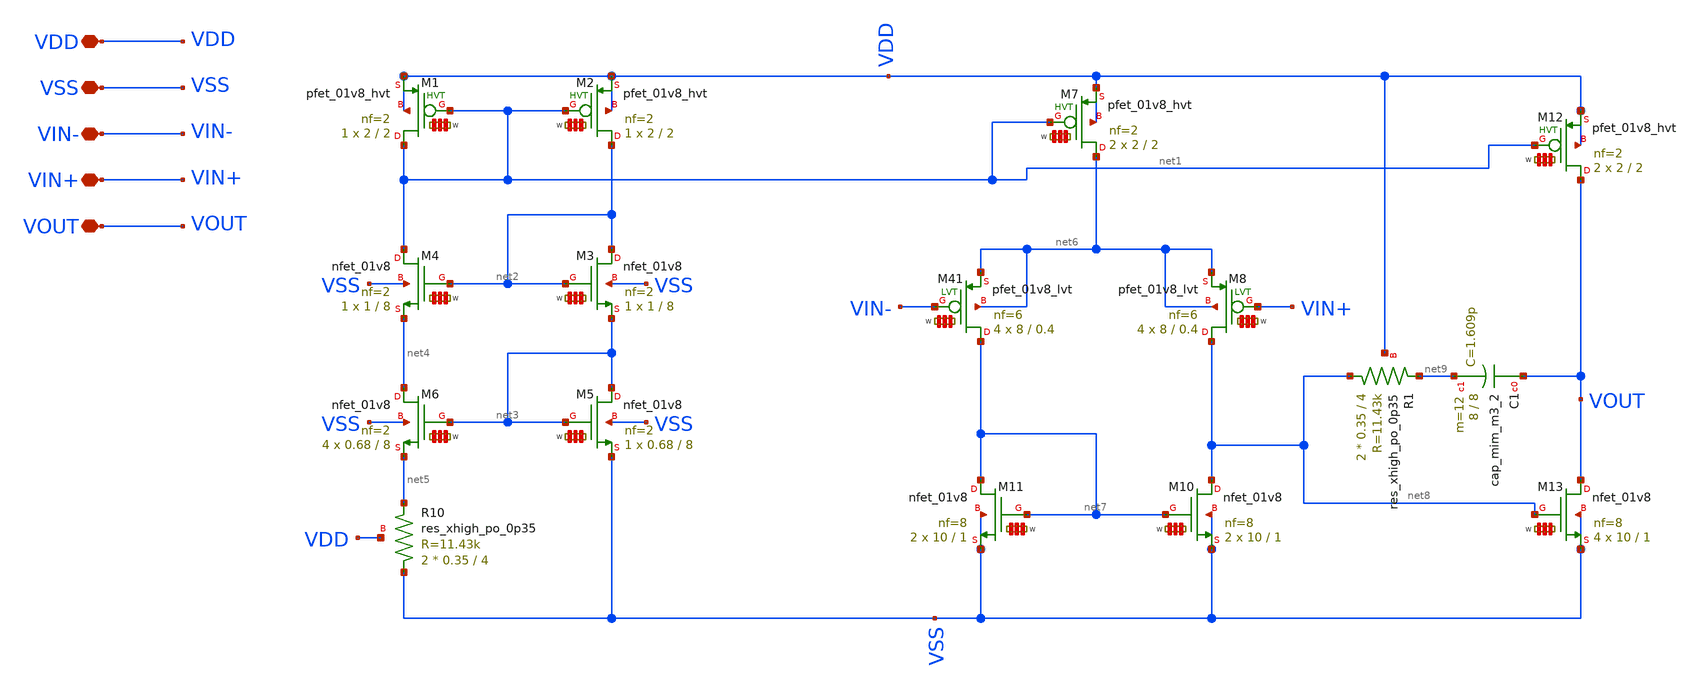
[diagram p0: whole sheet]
** sch_path: my_ip/sky130A/PMOS_2_stage_1_8_opamp_V1/op_amp.sch
**.subckt op_amp VDD VSS VIN- VIN+ VOUT
*.iopin VDD
*.iopin VSS
*.iopin VIN-
*.iopin VIN+
*.iopin VOUT
XM5 net3 net3 VSS VSS sky130_fd_pr__nfet_01v8 L=8 W='0.68 * 2 ' nf=2 ad='int((2 + 1)/2) * 0.68 / 2 * 0.29'
+ as='int((2 + 2)/2) * 0.68 / 2 * 0.29' pd='2*int((2 + 1)/2) * (0.68 / 2 + 0.29)' ps='2*int((2 + 2)/2) * (0.68 / 2 + 0.29)'
+ nrd='0.29 / 0.68 ' nrs='0.29 / 0.68 ' sa=0 sb=0 sd=0 mult=1 m=1
XM6 net4 net3 net5 VSS sky130_fd_pr__nfet_01v8 L=8 W='0.68 * 2 ' nf=2 ad='int((2 + 1)/2) * 0.68 / 2 * 0.29'
+ as='int((2 + 2)/2) * 0.68 / 2 * 0.29' pd='2*int((2 + 1)/2) * (0.68 / 2 + 0.29)' ps='2*int((2 + 2)/2) * (0.68 / 2 + 0.29)'
+ nrd='0.29 / 0.68 ' nrs='0.29 / 0.68 ' sa=0 sb=0 sd=0 mult=4 m=4
XM7 net6 net1 VDD VDD sky130_fd_pr__pfet_01v8_hvt L=2 W='2 * 2 ' nf=2 ad='int((2 + 1)/2) * 2 / 2 * 0.29'
+ as='int((2 + 2)/2) * 2 / 2 * 0.29' pd='2*int((2 + 1)/2) * (2 / 2 + 0.29)' ps='2*int((2 + 2)/2) * (2 / 2 + 0.29)'
+ nrd='0.29 / 2 ' nrs='0.29 / 2 ' sa=0 sb=0 sd=0 mult=2 m=2
XM2 net2 net1 VDD VDD sky130_fd_pr__pfet_01v8_hvt L=2 W='2 * 2 ' nf=2 ad='int((2 + 1)/2) * 2 / 2 * 0.29'
+ as='int((2 + 2)/2) * 2 / 2 * 0.29' pd='2*int((2 + 1)/2) * (2 / 2 + 0.29)' ps='2*int((2 + 2)/2) * (2 / 2 + 0.29)'
+ nrd='0.29 / 2 ' nrs='0.29 / 2 ' sa=0 sb=0 sd=0 mult=1 m=1
XM1 net1 net1 VDD VDD sky130_fd_pr__pfet_01v8_hvt L=2 W='2 * 2 ' nf=2 ad='int((2 + 1)/2) * 2 / 2 * 0.29'
+ as='int((2 + 2)/2) * 2 / 2 * 0.29' pd='2*int((2 + 1)/2) * (2 / 2 + 0.29)' ps='2*int((2 + 2)/2) * (2 / 2 + 0.29)'
+ nrd='0.29 / 2 ' nrs='0.29 / 2 ' sa=0 sb=0 sd=0 mult=1 m=1
XR10 VSS net5 VDD sky130_fd_pr__res_xhigh_po_0p35 L=4 mult=2 m=2
XM4 net1 net2 net4 VSS sky130_fd_pr__nfet_01v8 L=8 W='1 * 2 ' nf=2 ad='int((2 + 1)/2) * 1 / 2 * 0.29'
+ as='int((2 + 2)/2) * 1 / 2 * 0.29' pd='2*int((2 + 1)/2) * (1 / 2 + 0.29)' ps='2*int((2 + 2)/2) * (1 / 2 + 0.29)'
+ nrd='0.29 / 1 ' nrs='0.29 / 1 ' sa=0 sb=0 sd=0 mult=1 m=1
XM3 net2 net2 net3 VSS sky130_fd_pr__nfet_01v8 L=8 W='1 * 2 ' nf=2 ad='int((2 + 1)/2) * 1 / 2 * 0.29'
+ as='int((2 + 2)/2) * 1 / 2 * 0.29' pd='2*int((2 + 1)/2) * (1 / 2 + 0.29)' ps='2*int((2 + 2)/2) * (1 / 2 + 0.29)'
+ nrd='0.29 / 1 ' nrs='0.29 / 1 ' sa=0 sb=0 sd=0 mult=1 m=1
XM10 net8 net7 VSS VSS sky130_fd_pr__nfet_01v8 L=1 W='10 * 8 ' nf=8 ad='int((8 + 1)/2) * 10 / 8 * 0.29'
+ as='int((8 + 2)/2) * 10 / 8 * 0.29' pd='2*int((8 + 1)/2) * (10 / 8 + 0.29)' ps='2*int((8 + 2)/2) * (10 / 8 + 0.29)'
+ nrd='0.29 / 10 ' nrs='0.29 / 10 ' sa=0 sb=0 sd=0 mult=2 m=2
XM11 net7 net7 VSS VSS sky130_fd_pr__nfet_01v8 L=1 W='10 * 8 ' nf=8 ad='int((8 + 1)/2) * 10 / 8 * 0.29'
+ as='int((8 + 2)/2) * 10 / 8 * 0.29' pd='2*int((8 + 1)/2) * (10 / 8 + 0.29)' ps='2*int((8 + 2)/2) * (10 / 8 + 0.29)'
+ nrd='0.29 / 10 ' nrs='0.29 / 10 ' sa=0 sb=0 sd=0 mult=2 m=2
XM12 VOUT net1 VDD VDD sky130_fd_pr__pfet_01v8_hvt L=2 W='2 * 2 ' nf=2 ad='int((2 + 1)/2) * 2 / 2 * 0.29'
+ as='int((2 + 2)/2) * 2 / 2 * 0.29' pd='2*int((2 + 1)/2) * (2 / 2 + 0.29)' ps='2*int((2 + 2)/2) * (2 / 2 + 0.29)'
+ nrd='0.29 / 2 ' nrs='0.29 / 2 ' sa=0 sb=0 sd=0 mult=2 m=2
XM13 VOUT net8 VSS VSS sky130_fd_pr__nfet_01v8 L=1 W='10 * 8 ' nf=8 ad='int((8 + 1)/2) * 10 / 8 * 0.29'
+ as='int((8 + 2)/2) * 10 / 8 * 0.29' pd='2*int((8 + 1)/2) * (10 / 8 + 0.29)' ps='2*int((8 + 2)/2) * (10 / 8 + 0.29)'
+ nrd='0.29 / 10 ' nrs='0.29 / 10 ' sa=0 sb=0 sd=0 mult=4 m=4
XC1 VOUT net9 sky130_fd_pr__cap_mim_m3_2 W=8 L=8 MF=12 m=12
XR1 net8 net9 VDD sky130_fd_pr__res_xhigh_po_0p35 L=4 mult=2 m=2
XM41 net7 VIN- net6 net6 sky130_fd_pr__pfet_01v8_lvt L=0.4 W='8 * 6 ' nf=6 ad='int((6 + 1)/2) * 8 / 6 * 0.29'
+ as='int((6 + 2)/2) * 8 / 6 * 0.29' pd='2*int((6 + 1)/2) * (8 / 6 + 0.29)' ps='2*int((6 + 2)/2) * (8 / 6 + 0.29)'
+ nrd='0.29 / 8 ' nrs='0.29 / 8 ' sa=0 sb=0 sd=0 mult=4 m=4
XM8 net8 VIN+ net6 net6 sky130_fd_pr__pfet_01v8_lvt L=0.4 W='8 * 6 ' nf=6 ad='int((6 + 1)/2) * 8 / 6 * 0.29'
+ as='int((6 + 2)/2) * 8 / 6 * 0.29' pd='2*int((6 + 1)/2) * (8 / 6 + 0.29)' ps='2*int((6 + 2)/2) * (8 / 6 + 0.29)'
+ nrd='0.29 / 8 ' nrs='0.29 / 8 ' sa=0 sb=0 sd=0 mult=4 m=4
**.ends
.end
